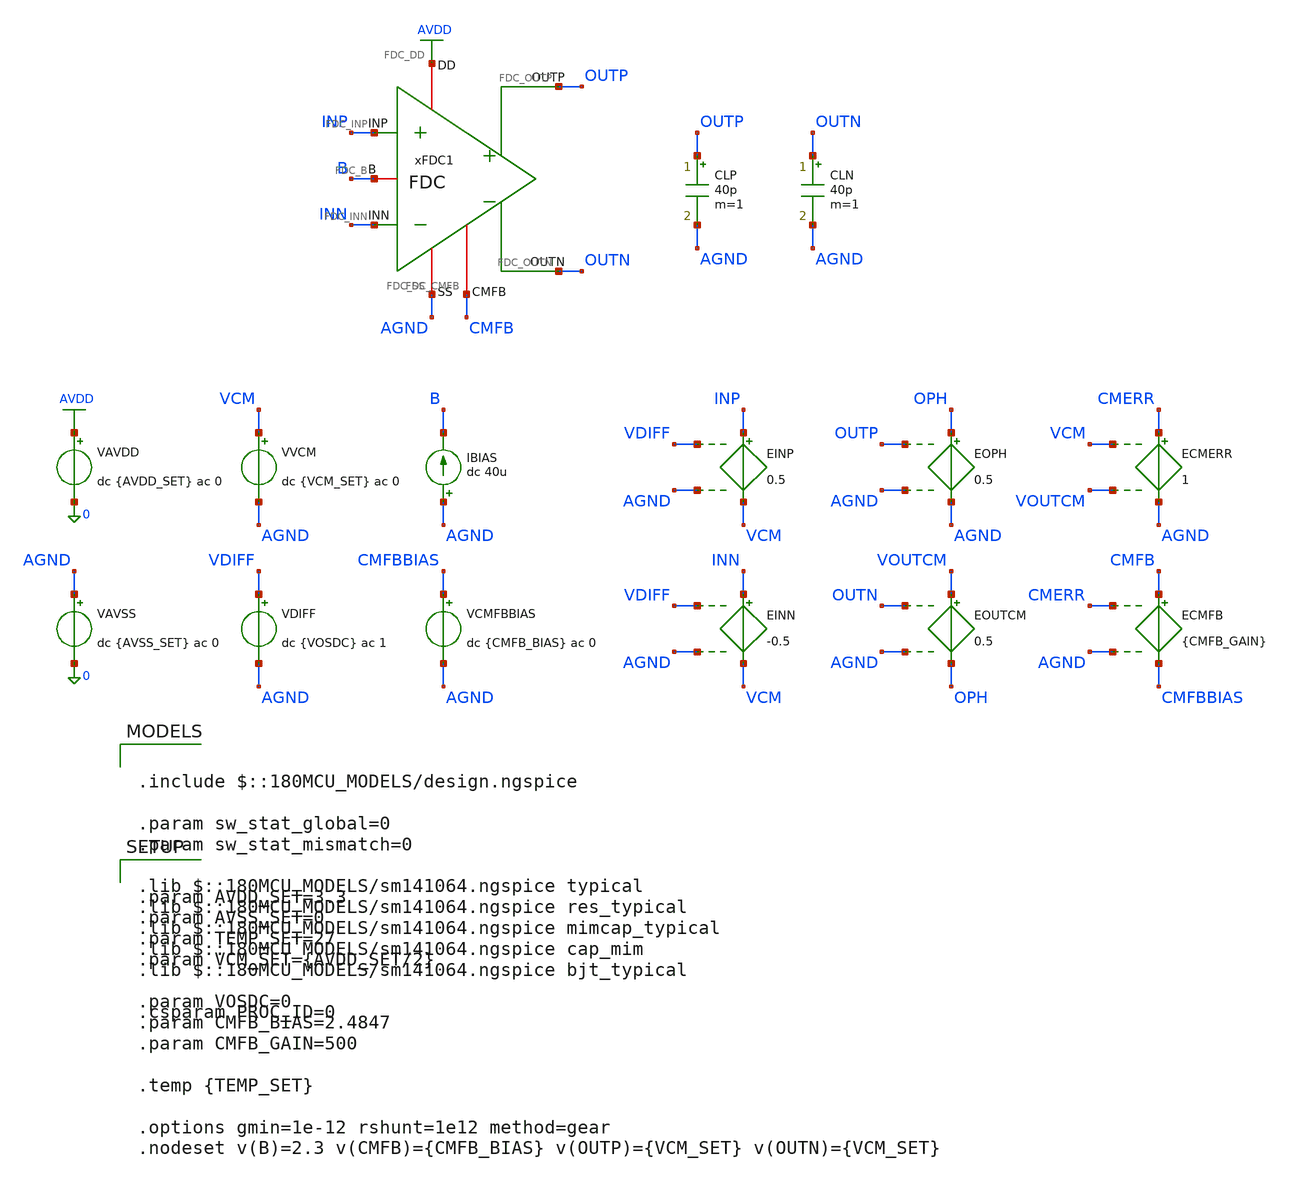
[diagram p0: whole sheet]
** sch_path: Design_Files/IC Design/Testbench/ANALOG_BLOCKS/FD_OTA/FDC/Open_Loop/FDC_TB_OL_NOM.sch
**.subckt FDC_TB_OL_NOM
IBIAS AGND B dc 40u
VAVDD AVDD 0 dc {AVDD_SET} ac 0
.save i(vavdd)
CLP OUTP AGND 40p m=1
VVCM VCM AGND dc {VCM_SET} ac 0
VDIFF VDIFF AGND dc {VOSDC} ac 1
VAVSS AGND 0 dc {AVSS_SET} ac 0
.save i(vavss)
EINN INN VCM VDIFF AGND -0.5
EINP INP VCM VDIFF AGND 0.5
CLN OUTN AGND 40p m=1
VCMFBBIAS CMFBBIAS AGND dc {CMFB_BIAS} ac 0
EOUTCM VOUTCM OPH OUTN AGND 0.5
EOPH OPH AGND OUTP AGND 0.5
ECMERR CMERR AGND VCM VOUTCM 1
ECMFB CMFB CMFBBIAS CMERR AGND {CMFB_GAIN}
xFDC1 AVDD AGND INP INN OUTN B OUTP CMFB FDC
**** begin user architecture code

.include $::180MCU_MODELS/design.ngspice

.param sw_stat_global=0
.param sw_stat_mismatch=0

.lib $::180MCU_MODELS/sm141064.ngspice typical
.lib $::180MCU_MODELS/sm141064.ngspice res_typical
.lib $::180MCU_MODELS/sm141064.ngspice mimcap_typical
.lib $::180MCU_MODELS/sm141064.ngspice cap_mim
.lib $::180MCU_MODELS/sm141064.ngspice bjt_typical

.csparam PROC_ID=0




.control

destroy all
save all

set wr_vecnames
set wr_singlescale

option numdgt=15


shell mkdir -p
+ /foss/designs/ECG_Acquisition_IC/Measurement_Results/IC_Simulation/ANALOG_BLOCKS/FD_OTA/FDC/NOM.Result_txt

shell rm -f
+ /foss/designs/ECG_Acquisition_IC/Measurement_Results/IC_Simulation/ANALOG_BLOCKS/FD_OTA/FDC/NOM.Result_txt/NOM.ol_op.txt
shell rm -f
+ /foss/designs/ECG_Acquisition_IC/Measurement_Results/IC_Simulation/ANALOG_BLOCKS/FD_OTA/FDC/NOM.Result_txt/NOM.ol_diff_ac.txt
shell rm -f
+ /foss/designs/ECG_Acquisition_IC/Measurement_Results/IC_Simulation/ANALOG_BLOCKS/FD_OTA/FDC/NOM.Result_txt/NOM.ol_offset.txt
shell rm -f
+ /foss/designs/ECG_Acquisition_IC/Measurement_Results/IC_Simulation/ANALOG_BLOCKS/FD_OTA/FDC/NOM.Result_txt/NOM.ol_noise.txt
shell rm -f
+ /foss/designs/ECG_Acquisition_IC/Measurement_Results/IC_Simulation/ANALOG_BLOCKS/FD_OTA/FDC/NOM.Result_txt/NOM.ol_noise_integrated.txt
shell rm -f
+ /foss/designs/ECG_Acquisition_IC/Measurement_Results/IC_Simulation/ANALOG_BLOCKS/FD_OTA/FDC/NOM.Result_txt/NOM.ol_diff_tran.txt
shell rm -f
+ /foss/designs/ECG_Acquisition_IC/Measurement_Results/IC_Simulation/ANALOG_BLOCKS/FD_OTA/FDC/NOM.Result_txt/NOM.ol_diff_cm_disturbance.txt


let avdd_run = 3.3
let vcm_run  = avdd_run/2
let vos_run  = 0


* OP

alter @VAVDD[DC] = $&avdd_run
alter @VVCM[DC]  = $&vcm_run
alter @VDIFF[DC] = $&vos_run

alter @VVCM[ACMAG]  = 0
alter @VDIFF[ACMAG] = 0
alter @VAVDD[ACMAG] = 0
alter @VAVSS[ACMAG] = 0

op

let op_vdd     = v(avdd)-v(agnd)
let op_vinp    = v(inp)-v(agnd)
let op_vinn    = v(inn)-v(agnd)
let op_vid     = op_vinp-op_vinn

let op_voutp   = v(outp)-v(agnd)
let op_voutn   = v(outn)-v(agnd)
let op_voutcm  = (op_voutp+op_voutn)/2
let op_vod     = op_voutp-op_voutn

let op_ibias   = 40e-6
let op_idd     = -vavdd#branch
let op_power   = -(v(avdd)*vavdd#branch+v(agnd)*vavss#branch)
let op_cmfb    = v(cmfb)-v(agnd)

wrdata
+ /foss/designs/ECG_Acquisition_IC/Measurement_Results/IC_Simulation/ANALOG_BLOCKS/FD_OTA/FDC/NOM.Result_txt/NOM.ol_op.txt op_vdd op_vinp op_vinn op_vid op_voutp op_voutn op_voutcm op_vod op_ibias op_idd op_power op_cmfb


* Differential AC

alter @VVCM[DC]  = $&vcm_run
alter @VDIFF[DC] = $&vos_run

alter @VVCM[ACMAG]   = 0
alter @VDIFF[ACMAG]  = 1
alter @VDIFF[ACPHASE] = 0
alter @VAVDD[ACMAG]  = 0
alter @VAVSS[ACMAG]  = 0

ac dec 200 1 1G

let vid_ac  = v(inp)-v(inn)
let vod_ac  = v(outp)-v(outn)
let ad_ac   = vod_ac/vid_ac
let ad_real = real(ad_ac)
let ad_imag = imag(ad_ac)

setscale frequency

wrdata
+ /foss/designs/ECG_Acquisition_IC/Measurement_Results/IC_Simulation/ANALOG_BLOCKS/FD_OTA/FDC/NOM.Result_txt/NOM.ol_diff_ac.txt ad_real ad_imag


* Offset

alter @VVCM[DC] = $&vcm_run

alter @VVCM[ACMAG]  = 0
alter @VDIFF[ACMAG] = 0
alter @VAVDD[ACMAG] = 0
alter @VAVSS[ACMAG] = 0

dc VDIFF -0.02 0.02 1e-5

let off_vdiff  = v(vdiff)-v(agnd)
let off_vinp   = v(inp)-v(agnd)
let off_vinn   = v(inn)-v(agnd)

let off_voutp  = v(outp)-v(agnd)
let off_voutn  = v(outn)-v(agnd)
let off_voutcm = (off_voutp+off_voutn)/2
let off_vod    = off_voutp-off_voutn

let off_idd    = -vavdd#branch
let off_cmfb   = v(cmfb)-v(agnd)

setscale off_vdiff

wrdata
+ /foss/designs/ECG_Acquisition_IC/Measurement_Results/IC_Simulation/ANALOG_BLOCKS/FD_OTA/FDC/NOM.Result_txt/NOM.ol_offset.txt off_vinp off_vinn off_voutp off_voutn off_voutcm off_vod off_idd off_cmfb


* Integrated noise

alter @VVCM[DC]  = $&vcm_run
alter @VDIFF[DC] = $&vos_run

alter @VVCM[ACMAG]   = 0
alter @VDIFF[ACMAG]  = 1
alter @VDIFF[ACPHASE] = 0
alter @VAVDD[ACMAG]  = 0
alter @VAVSS[ACMAG]  = 0

noise v(outp,outn) VDIFF dec 100 0.05 150

setplot noise2

let input_noise_Vrms  = inoise_total
let output_noise_Vrms = onoise_total

echo f_low_Hz f_high_Hz input_noise_Vrms output_noise_Vrms >
+ /foss/designs/ECG_Acquisition_IC/Measurement_Results/IC_Simulation/ANALOG_BLOCKS/FD_OTA/FDC/NOM.Result_txt/NOM.ol_noise_integrated.txt
echo 0.05 150 $&input_noise_Vrms $&output_noise_Vrms >>
+ /foss/designs/ECG_Acquisition_IC/Measurement_Results/IC_Simulation/ANALOG_BLOCKS/FD_OTA/FDC/NOM.Result_txt/NOM.ol_noise_integrated.txt


* Noise density

noise v(outp,outn) VDIFF dec 100 0.01 10Meg

setplot noise3

let input_noise_VrtHz  = inoise_spectrum
let output_noise_VrtHz = onoise_spectrum

setscale frequency

wrdata
+ /foss/designs/ECG_Acquisition_IC/Measurement_Results/IC_Simulation/ANALOG_BLOCKS/FD_OTA/FDC/NOM.Result_txt/NOM.ol_noise.txt input_noise_VrtHz output_noise_VrtHz


* Differential-step CM disturbance

alter @VAVDD[DC] = $&avdd_run
alter @VVCM[DC]  = $&vcm_run

alter @VDIFF[PWL]=[ 0 0 1u 0 1.001u 50u 11u 50u 11.001u 0 21u 0 21.001u -50u 31u -50u 31.001u 0 40u
+ 0 ]

tran 5n 40u

let tr_vdiff  = v(vdiff)-v(agnd)

let tr_vinp   = v(inp)-v(agnd)
let tr_vinn   = v(inn)-v(agnd)
let tr_vid    = tr_vinp-tr_vinn

let tr_voutp  = v(outp)-v(agnd)
let tr_voutn  = v(outn)-v(agnd)

let tr_voutcm = (tr_voutp+tr_voutn)/2
let tr_vod    = tr_voutp-tr_voutn

let tr_cmfb   = v(cmfb)-v(agnd)
let tr_idd    = -vavdd#branch

meas tran cm_base AVG tr_voutcm FROM=0.2u TO=0.9u

let tr_cm_base = 0*tr_voutcm+cm_base
let tr_cm_delta = abs(tr_voutcm-cm_base)

meas tran cm_disturbance MAX tr_cm_delta FROM=1u TO=31.1u

setscale time

wrdata
+ /foss/designs/ECG_Acquisition_IC/Measurement_Results/IC_Simulation/ANALOG_BLOCKS/FD_OTA/FDC/NOM.Result_txt/NOM.ol_diff_tran.txt tr_vdiff tr_vid tr_voutp tr_voutn tr_voutcm tr_vod tr_cm_base tr_cm_delta tr_idd tr_cmfb

echo cm_base_V cm_disturbance_V >
+ /foss/designs/ECG_Acquisition_IC/Measurement_Results/IC_Simulation/ANALOG_BLOCKS/FD_OTA/FDC/NOM.Result_txt/NOM.ol_diff_cm_disturbance.txt
echo $&cm_base $&cm_disturbance >>
+ /foss/designs/ECG_Acquisition_IC/Measurement_Results/IC_Simulation/ANALOG_BLOCKS/FD_OTA/FDC/NOM.Result_txt/NOM.ol_diff_cm_disturbance.txt


quit

.endc




.param AVDD_SET=3.3
.param AVSS_SET=0
.param TEMP_SET=27
.param VCM_SET={AVDD_SET/2}

.param VOSDC=0
.param CMFB_BIAS=2.4847
.param CMFB_GAIN=500

.temp {TEMP_SET}

.options gmin=1e-12 rshunt=1e12 method=gear
.nodeset v(B)=2.3 v(CMFB)={CMFB_BIAS} v(OUTP)={VCM_SET} v(OUTN)={VCM_SET}


**** end user architecture code
**.ends
.GLOBAL AVDD
.end
